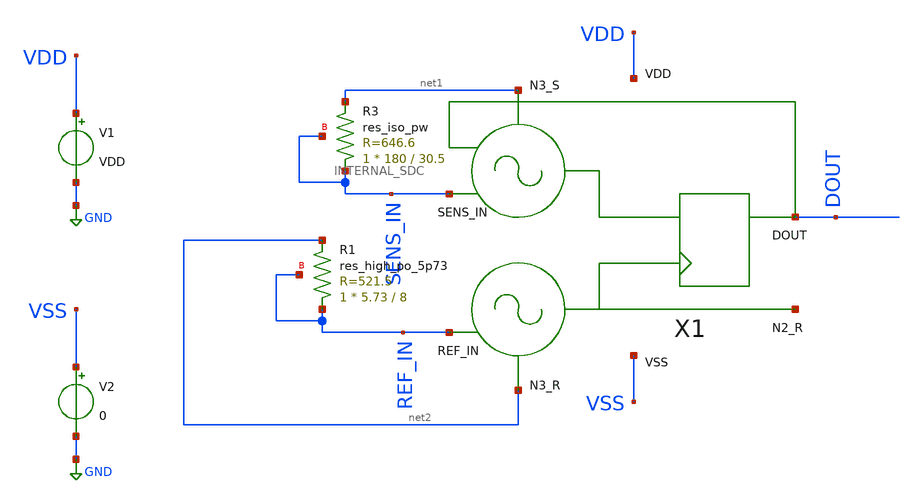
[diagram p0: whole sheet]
** sch_path: modules/INTERNAL_SDC/test/transient.sch

.include $::SKYWATER_STDCELLS/sky130_fd_sc_hd.spice

**.subckt transient
V1 VDD GND VDD
V2 VSS GND 0
X1 SENS_IN REF_IN DOUT VDD VSS net1 net2 net3 INTERNAL_SDC
XR1 REF_IN net2 REF_IN sky130_fd_pr__res_high_po_5p73 L=8 mult=1 m=1
XR3 SENS_IN net1 SENS_IN sky130_fd_pr__res_iso_pw W=180 L=30.5 m=1
**** begin user architecture code


.param VDD = 1.8
.ic v(SENS_IN) = 0
.ic v(REF_IN) = 1.8
.option temp = -40
.save v(DOUT)
.control
  run
compose vin_var start=2.05k stop=2.05k step=0.02k
foreach val $&vin_var
  alter R_SENS $val
  tran 0.1n 20u
*  tran 0.1n 50u
end
*plot tran1.v(N2) tran2.v(N2) tran3.v(N2) tran4.v(N2) tran5.v(N2) tran6.v(N2) tran7.v(N2)
*+ tran8.v(N2) tran9.v(N2) tran10.v(N2) tran11.v(N2)
*wrdata ringosc_CINsweep_v2p1_Creal.txt tran1.v(N2) tran2.v(N2) tran3.v(N2) tran4.v(N2) tran5.v(N2)
*+ tran6.v(N2) tran7.v(N2) tran8.v(N2) tran9.v(N2) tran10.v(N2) tran11.v(N2)
*wrdata SDC_CINsweep_v5p7.txt tran1.v(DOUT) tran2.v(DOUT) tran3.v(DOUT) tran4.v(DOUT) tran5.v(DOUT)
*+ tran6.v(DOUT) tran7.v(DOUT) tran8.v(DOUT) tran9.v(DOUT) tran10.v(DOUT) tran11.v(DOUT) tran12.v(DOUT)
*+ tran13.v(DOUT) tran14.v(DOUT) tran15.v(DOUT) tran16.v(DOUT)
*wrdata SDC_RINsweep_v2p1_CLOAD.txt tran1.v(DOUT_CLOAD) tran2.v(DOUT_CLOAD) tran3.v(DOUT_CLOAD)
*+ tran4.v(DOUT_CLOAD) tran5.v(DOUT_CLOAD) tran6.v(DOUT_CLOAD) tran7.v(DOUT_CLOAD) tran8.v(DOUT_CLOAD) tran9.v(DOUT_CLOAD)
*+ tran10.v(DOUT_CLOAD) tran11.v(DOUT_CLOAD) tran12.v(DOUT_CLOAD) tran13.v(DOUT_CLOAD) tran14.v(DOUT_CLOAD)
*+ tran15.v(DOUT_CLOAD) tran16.v(DOUT_CLOAD)
*wrdata SDC_CINsweep_v5p7_CLOAD.txt tran1.v(DOUT_CLOAD)
wrdata SDC_RINsweep_v9p1_CLOAD_tm40.txt tran1.v(DOUT)
.endc


.lib $env(PDK_ROOT)/$env(PDK)/libs.tech/ngspice/sky130.lib.spice.tt.red tt
*.lib $env(PDK_ROOT)/$env(PDK)/libs.tech/combined/sky130.lib.spice tt

**** end user architecture code
**.ends
.GLOBAL GND
.end
